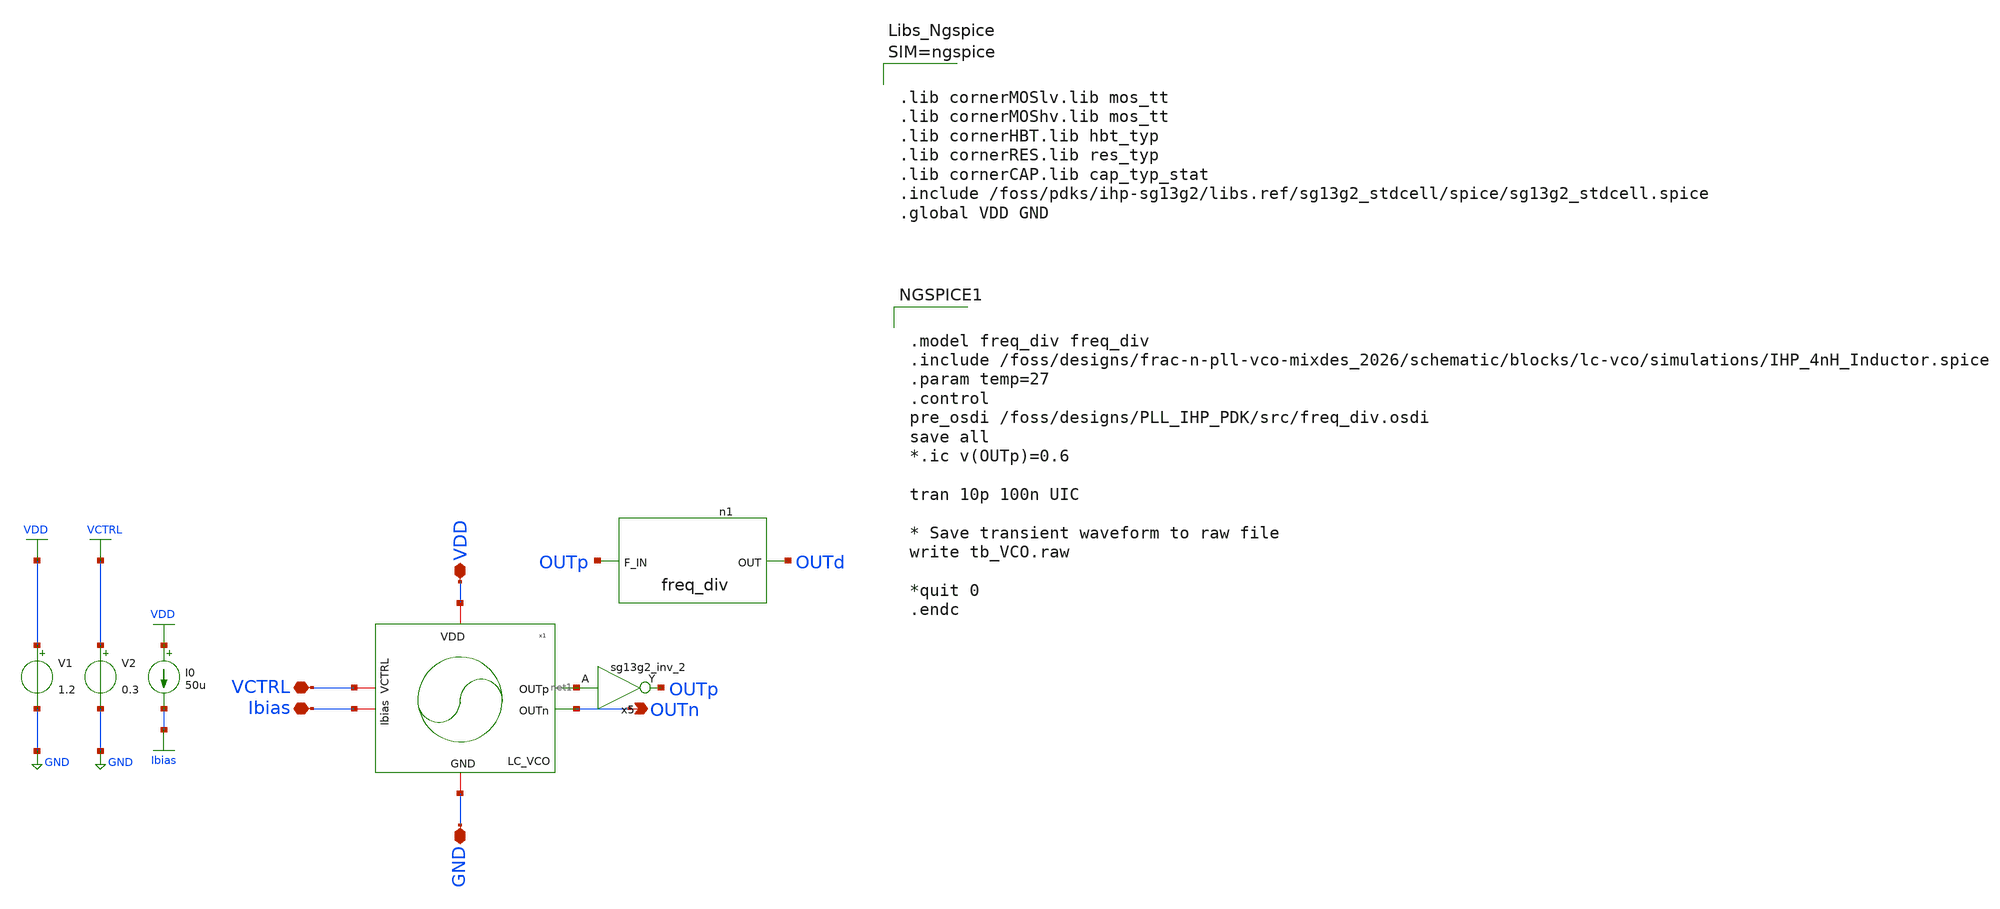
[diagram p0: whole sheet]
** sch_path: tb/tb_VCO.sch
**.subckt tb_VCO OUTn VDD VCTRL GND Ibias
*.opin OUTn
*.iopin VDD
*.iopin VCTRL
*.iopin GND
*.iopin Ibias
V1 VDD GND 1.2
V2 VCTRL GND 0.3
I0 VDD Ibias 50u
x2 VDD net1 OUTn Ibias VCTRL GND LC_VCO
n1 OUTd OUTp freq_div
x5 OUTp net1 VDD GND sg13g2_inv_2
**** begin user architecture code


.model freq_div freq_div
.include /foss/designs/frac-n-pll-vco-mixdes_2026/schematic/blocks/lc-vco/simulations/IHP_4nH_Inductor.spice
.param temp=27
.control
pre_osdi /foss/designs/PLL_IHP_PDK/src/freq_div.osdi
save all
*.ic v(OUTp)=0.6

tran 10p 100n UIC

* Save transient waveform to raw file
write tb_VCO.raw

*quit 0
.endc





.lib cornerMOSlv.lib mos_tt
.lib cornerMOShv.lib mos_tt
.lib cornerHBT.lib hbt_typ
.lib cornerRES.lib res_typ
.lib cornerCAP.lib cap_typ_stat
.include /foss/pdks/ihp-sg13g2/libs.ref/sg13g2_stdcell/spice/sg13g2_stdcell.spice
.global VDD GND




**** end user architecture code
**.ends
.GLOBAL GND
.GLOBAL VDD
.GLOBAL VCTRL
.GLOBAL Ibias
.end
